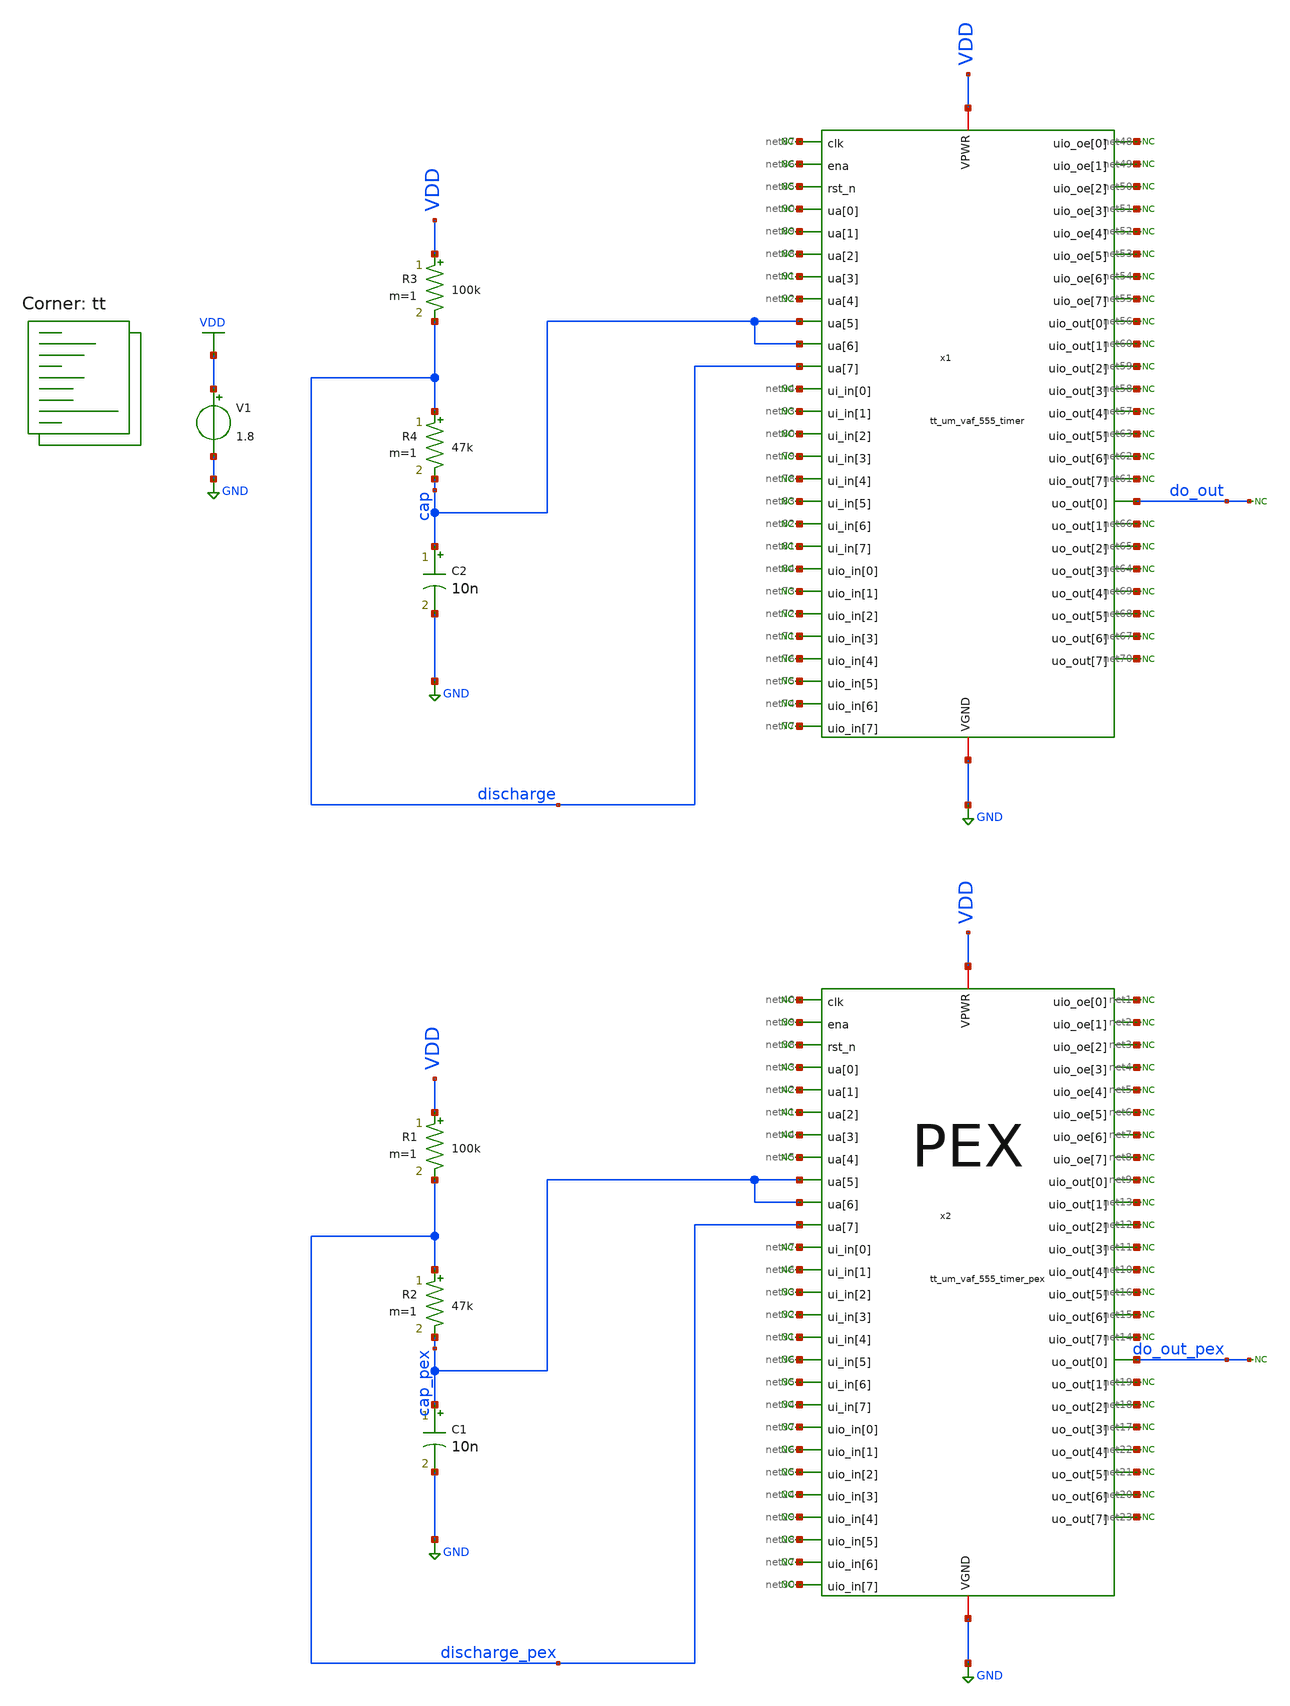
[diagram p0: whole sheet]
** sch_path: xsch/tb/tt_um_vaf_555_timer/tb_tt_um_vaf_555_timer_astable.sch
**.subckt tb_tt_um_vaf_555_timer_astable
V1 VDD GND 1.8
.save i(v1)
R1 VDD discharge_pex 100k m=1
R2 discharge_pex cap_pex 47k m=1
C1 cap_pex GND 10n m=1
* noconn do_out_pex
* noconn #net1
* noconn #net2
* noconn #net3
* noconn #net4
* noconn #net5
* noconn #net6
* noconn #net7
* noconn #net8
* noconn #net9
* noconn #net10
* noconn #net11
* noconn #net12
* noconn #net13
* noconn #net14
* noconn #net15
* noconn #net16
* noconn #net17
* noconn #net18
* noconn #net19
* noconn #net20
* noconn #net21
* noconn #net22
* noconn #net23
* noconn #net24
* noconn #net25
* noconn #net26
* noconn #net27
* noconn #net28
* noconn #net29
* noconn #net30
* noconn #net31
* noconn #net32
* noconn #net33
* noconn #net34
* noconn #net35
* noconn #net36
* noconn #net37
* noconn #net38
* noconn #net39
* noconn #net40
* noconn #net41
* noconn #net42
* noconn #net43
* noconn #net44
* noconn #net45
* noconn #net46
* noconn #net47
x2 net40 net39 net38 net43 net42 net41 net44 net45 cap_pex cap_pex discharge_pex net47 net46 net33
+ net32 net31 net36 net35 net34 net37 net26 net25 net24 net29 net28 net27 net30 net1 net2 net3 net4 net5
+ net6 net7 net8 net9 net13 net12 net11 net10 net16 net15 net14 do_out_pex net19 net18 net17 net22 net21
+ net20 net23 VDD GND tt_um_vaf_555_timer_pex
R3 VDD discharge 100k m=1
R4 discharge cap 47k m=1
C2 cap GND 10n m=1
* noconn do_out
* noconn #net48
* noconn #net49
* noconn #net50
* noconn #net51
* noconn #net52
* noconn #net53
* noconn #net54
* noconn #net55
* noconn #net56
* noconn #net57
* noconn #net58
* noconn #net59
* noconn #net60
* noconn #net61
* noconn #net62
* noconn #net63
* noconn #net64
* noconn #net65
* noconn #net66
* noconn #net67
* noconn #net68
* noconn #net69
* noconn #net70
* noconn #net71
* noconn #net72
* noconn #net73
* noconn #net74
* noconn #net75
* noconn #net76
* noconn #net77
* noconn #net78
* noconn #net79
* noconn #net80
* noconn #net81
* noconn #net82
* noconn #net83
* noconn #net84
* noconn #net85
* noconn #net86
* noconn #net87
* noconn #net88
* noconn #net89
* noconn #net90
* noconn #net91
* noconn #net92
* noconn #net93
* noconn #net94
x1 net87 net86 net85 net90 net89 net88 net91 net92 cap cap discharge net94 net93 net80 net79 net78
+ net83 net82 net81 net84 net73 net72 net71 net76 net75 net74 net77 net48 net49 net50 net51 net52 net53
+ net54 net55 net56 net60 net59 net58 net57 net63 net62 net61 do_out net66 net65 net64 net69 net68 net67
+ net70 VDD GND tt_um_vaf_555_timer
**** begin user architecture code



.ic v(cap) = 0
.ic v(cap_pex) = 0

.control
	tran 1u 10m

	plot v(cap) v(cap_pex)

.endc
.end


.lib $::SKYWATER_MODELS/sky130.lib.spice tt


.save v(do_out) v(discharge) v(cap) v(cap_pex)
=

.savecurrents




.include ~/projects/tt06_555/xsch/ip/top/tt_um_vaf_555_timer/tt_um_vaf_555_timer_pex.spice


**** end user architecture code
**.ends
.GLOBAL VDD
.GLOBAL GND
.end
